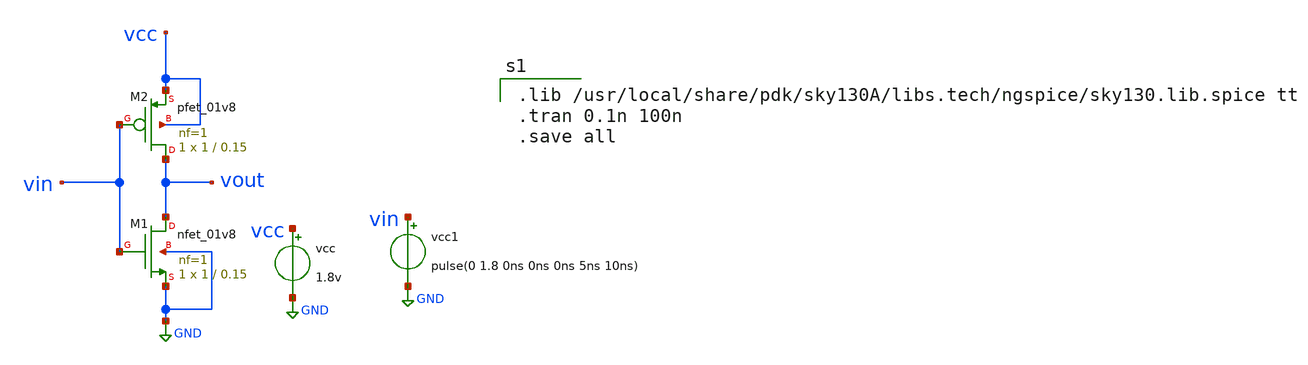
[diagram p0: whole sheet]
** sch_path: first.sch
**.subckt first
vcc1 vin GND pulse(0 1.8 0ns 0ns 0ns 5ns 10ns)
vcc vcc GND 1.8v
XM1 vout vin GND GND sky130_fd_pr__nfet_01v8 L=0.15 W=1 nf=1 ad='int((nf+1)/2) * W/nf * 0.29' as='int((nf+2)/2) * W/nf * 0.29'
+ pd='2*int((nf+1)/2) * (W/nf + 0.29)' ps='2*int((nf+2)/2) * (W/nf + 0.29)' nrd='0.29 / W' nrs='0.29 / W'
+ sa=0 sb=0 sd=0 mult=1 m=1
XM2 vout vin vcc vcc sky130_fd_pr__pfet_01v8 L=0.15 W=1 nf=1 ad='int((nf+1)/2) * W/nf * 0.29' as='int((nf+2)/2) * W/nf * 0.29'
+ pd='2*int((nf+1)/2) * (W/nf + 0.29)' ps='2*int((nf+2)/2) * (W/nf + 0.29)' nrd='0.29 / W' nrs='0.29 / W'
+ sa=0 sb=0 sd=0 mult=1 m=1
**** begin user architecture code

.lib /usr/local/share/pdk/sky130A/libs.tech/ngspice/sky130.lib.spice tt
.tran 0.1n 100n
.save all

**** end user architecture code
**.ends
.GLOBAL GND
.end
